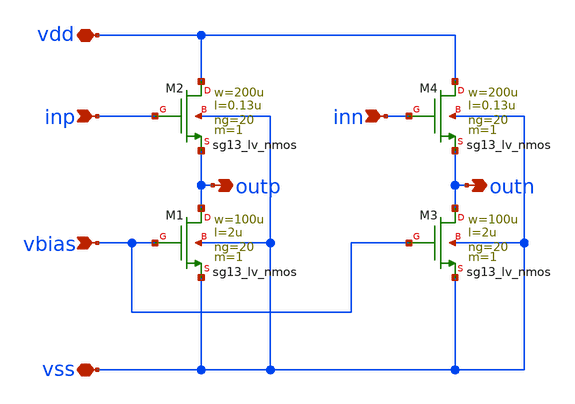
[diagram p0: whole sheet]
** sch_path: examples/source_follower/sch/source_follower.sch
**.subckt source_follower vbias vdd outp vss outn inp inn
*.ipin vbias
*.iopin vdd
*.opin outp
*.iopin vss
*.opin outn
*.ipin inp
*.ipin inn
XM1 outp vbias vss vss sg13_lv_nmos w=100u l=2u ng=20 m=1 mm_ok=1
XM2 vdd inp outp vss sg13_lv_nmos w=200u l=0.13u ng=20 m=1 mm_ok=1
XM3 outn vbias vss vss sg13_lv_nmos w=100u l=2u ng=20 m=1 mm_ok=1
XM4 vdd inn outn vss sg13_lv_nmos w=200u l=0.13u ng=20 m=1 mm_ok=1
**.ends
.end
